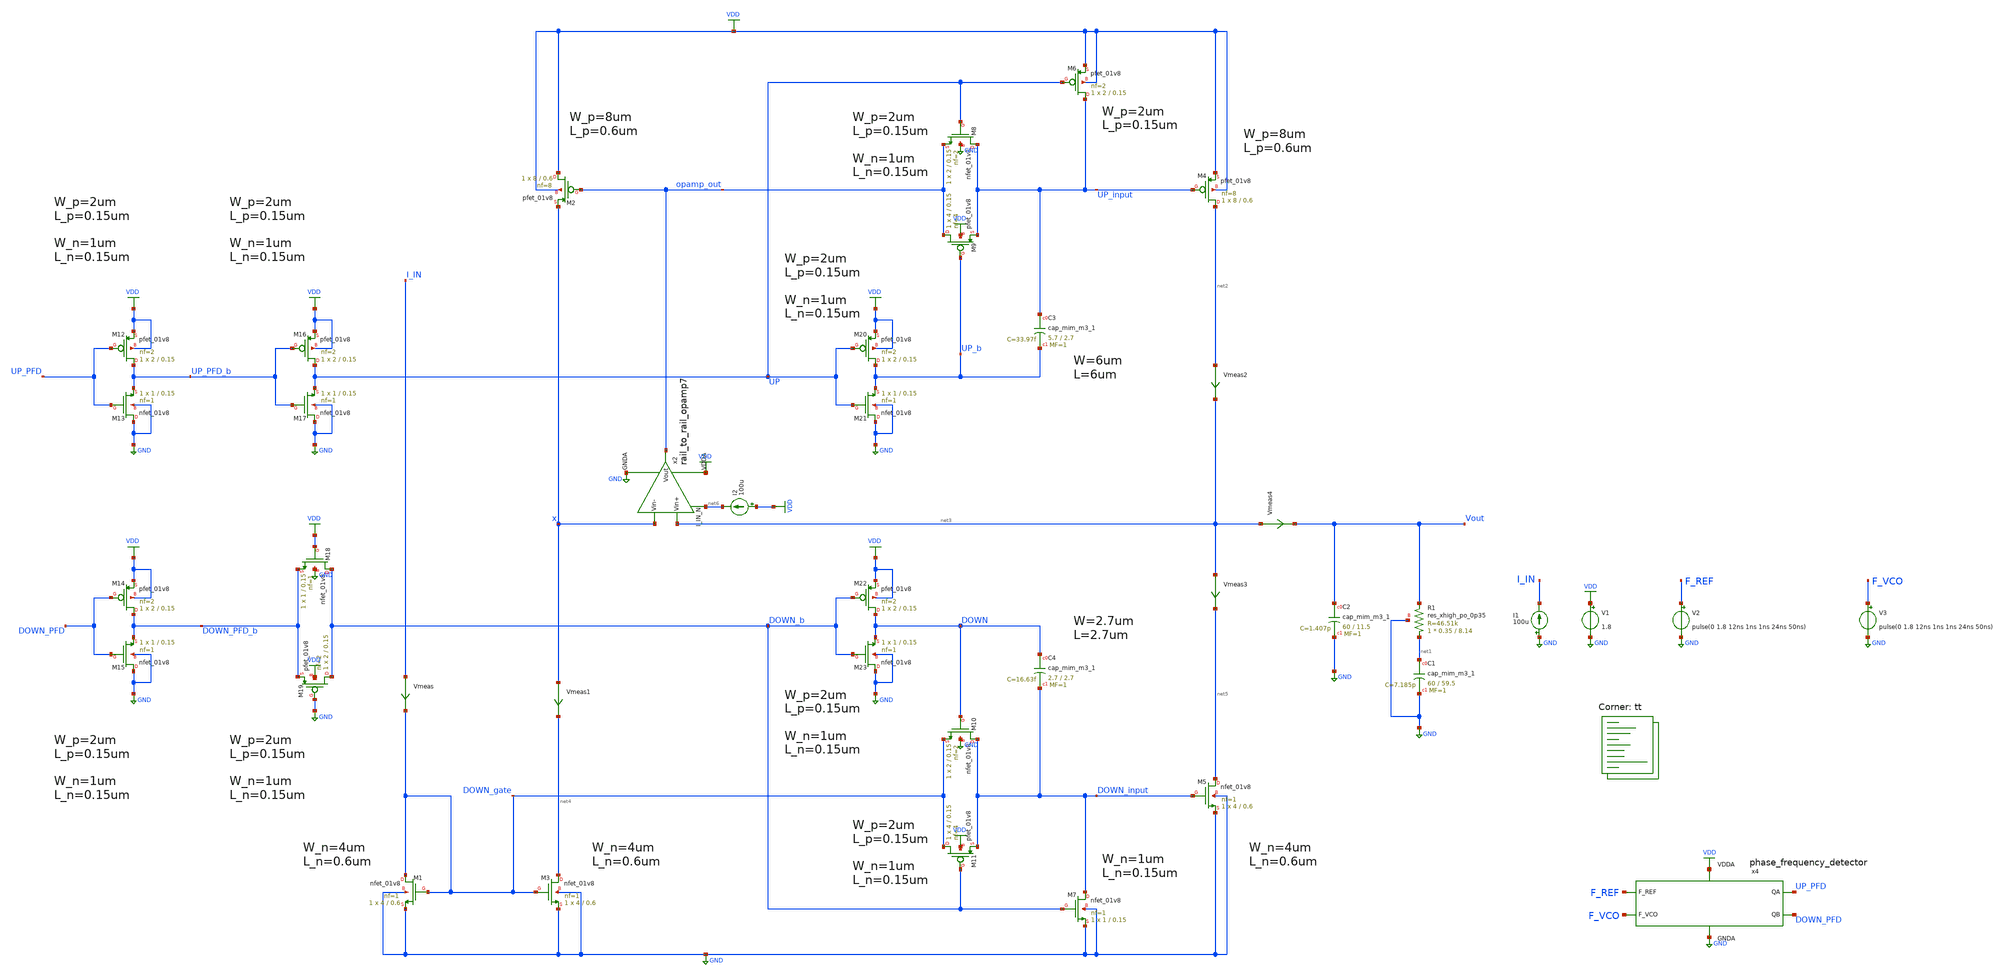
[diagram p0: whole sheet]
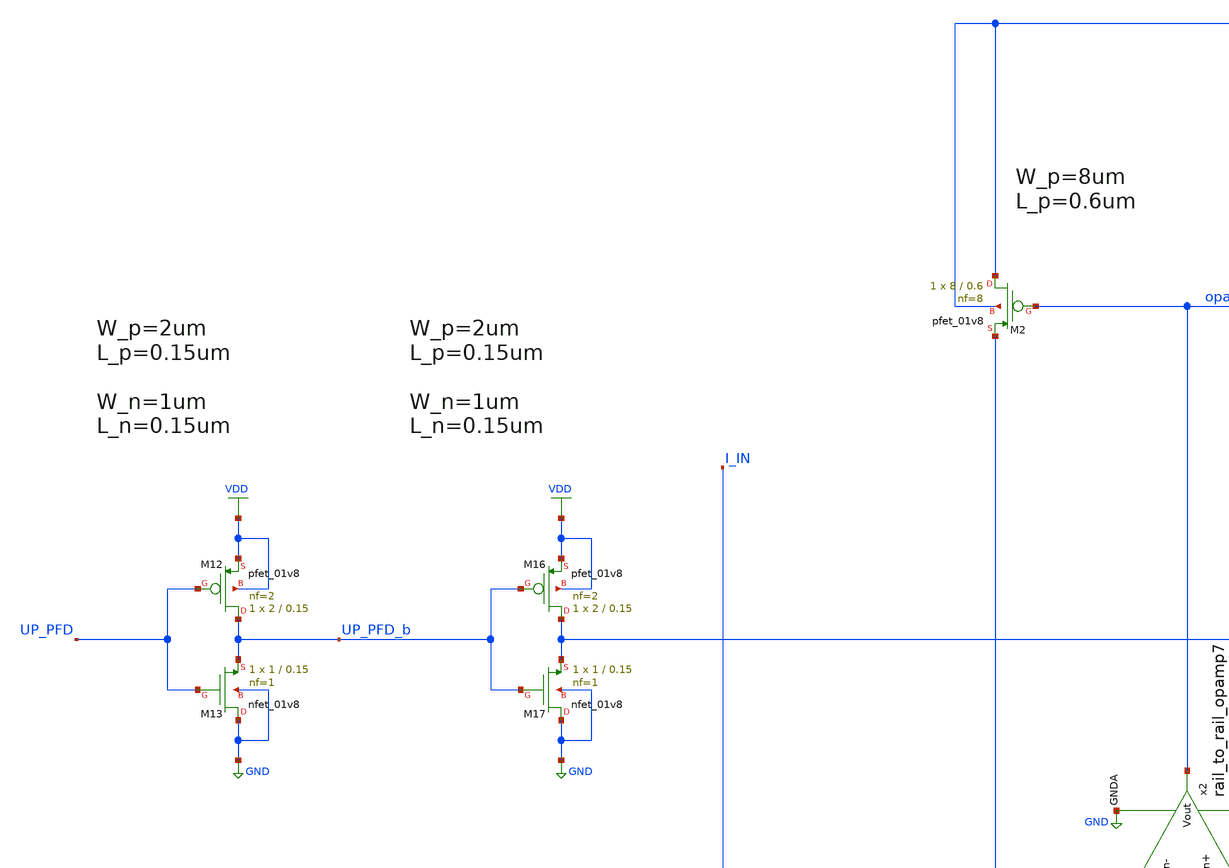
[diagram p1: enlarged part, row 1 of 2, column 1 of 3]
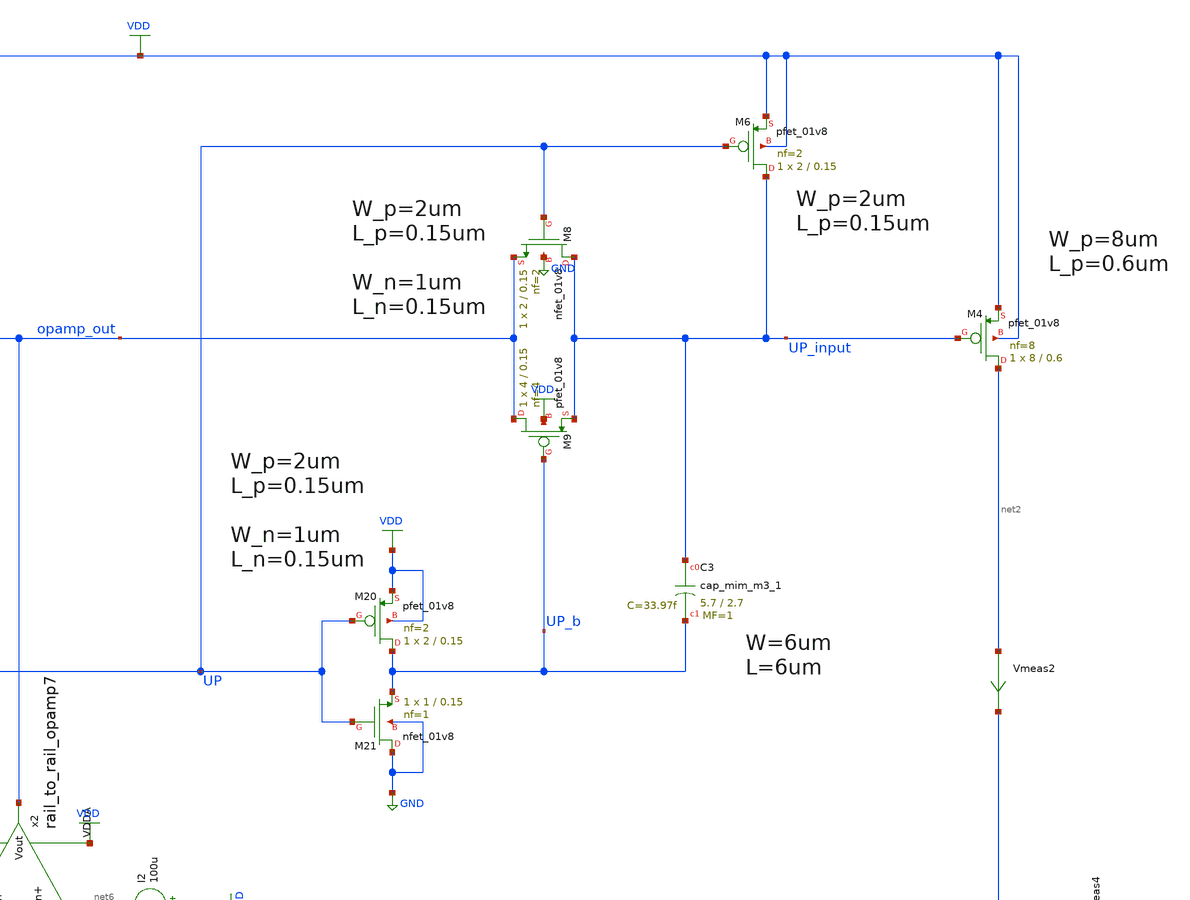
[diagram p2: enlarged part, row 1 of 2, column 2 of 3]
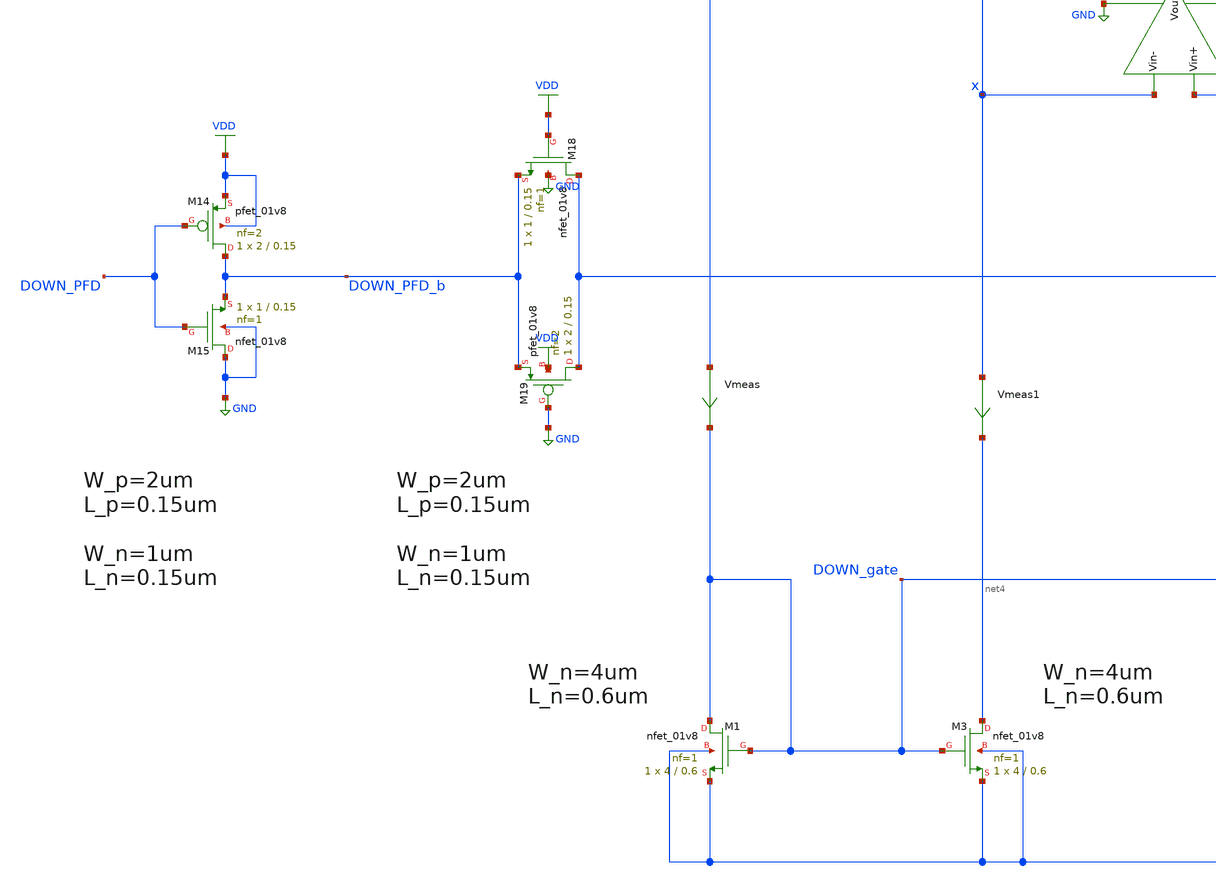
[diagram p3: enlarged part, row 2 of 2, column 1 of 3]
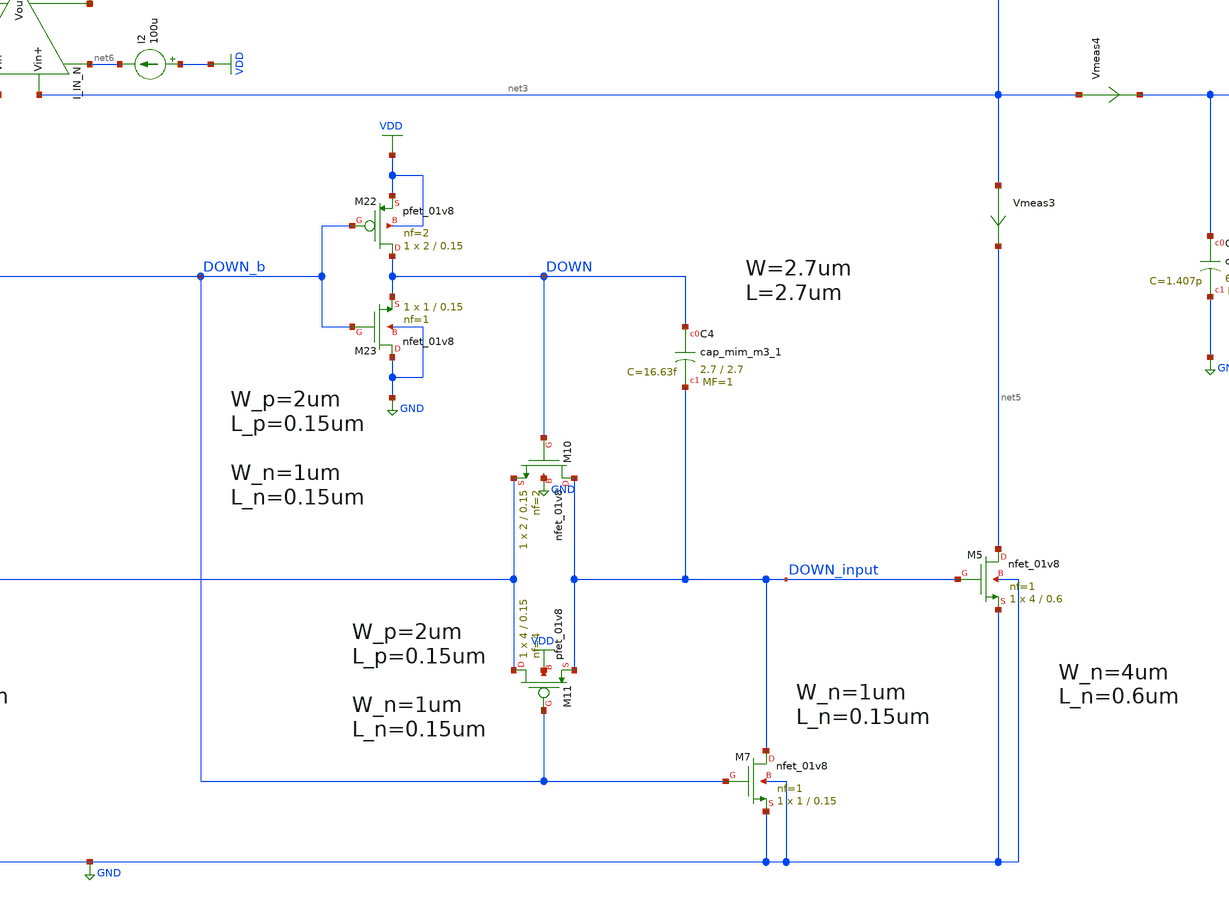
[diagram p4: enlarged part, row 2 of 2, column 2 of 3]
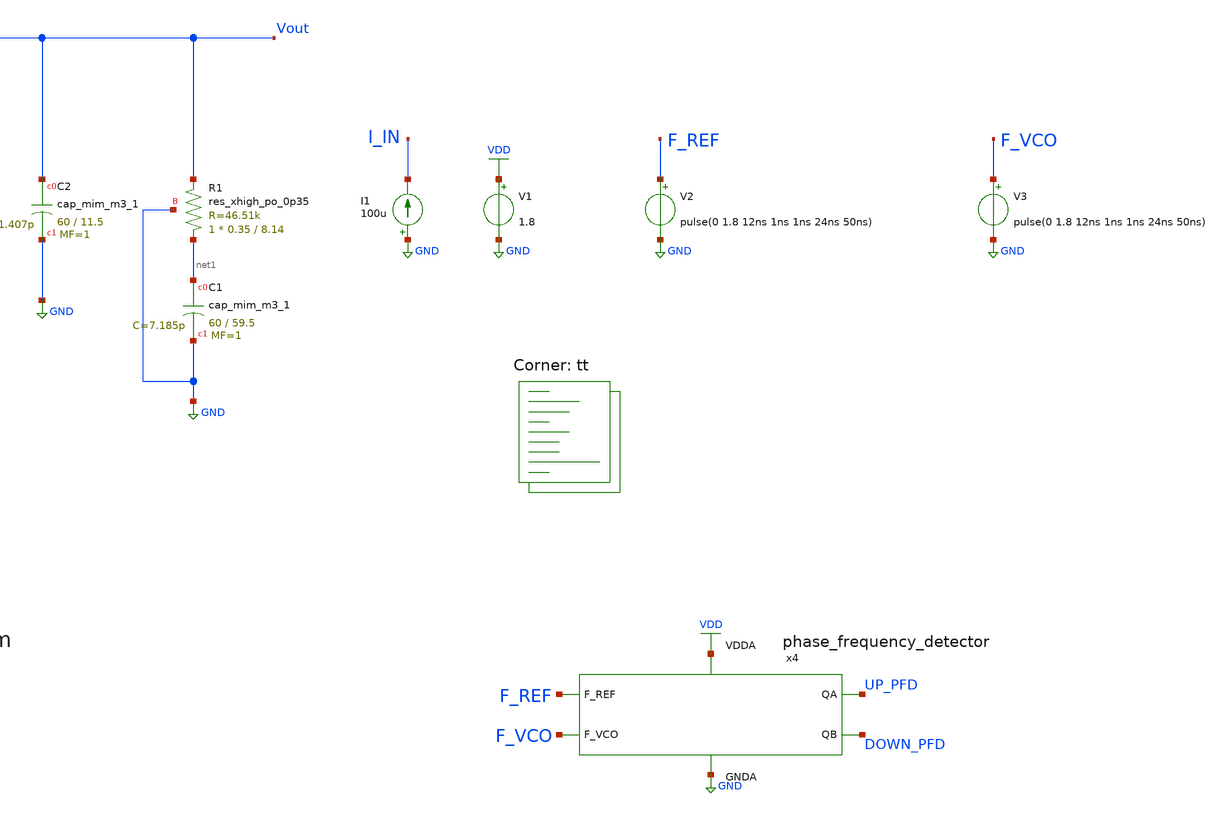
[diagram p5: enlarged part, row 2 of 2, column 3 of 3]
** sch_path: projects/pll/charge_pump/xschem_ngspice/pfd_charge_pump_13.sch
**.subckt pfd_charge_pump_13
V1 VDD GND 1.8
XC2 Vout GND sky130_fd_pr__cap_mim_m3_1 W=60 L=11.5 MF=1 m=1
XC1 net1 GND sky130_fd_pr__cap_mim_m3_1 W=60 L=59.5 MF=1 m=1
V2 F_REF GND pulse(0 1.8 12ns 1ns 1ns 24ns 50ns)
V3 F_VCO GND pulse(0 1.8 12ns 1ns 1ns 24ns 50ns)
x4 F_REF F_VCO VDD UP_PFD DOWN_PFD GND phase_frequency_detector
XR1 net1 Vout GND sky130_fd_pr__res_xhigh_po_0p35 L=8.14 mult=1 m=1
I1 GND I_IN 100u
Vmeas3 net3 net5 0
.save i(vmeas3)
XM1 DOWN_gate DOWN_gate GND GND sky130_fd_pr__nfet_01v8 L=0.6 W=4 nf=1 ad='int((nf+1)/2) * W/nf * 0.29'
+ as='int((nf+2)/2) * W/nf * 0.29' pd='2*int((nf+1)/2) * (W/nf + 0.29)' ps='2*int((nf+2)/2) * (W/nf + 0.29)'
+ nrd='0.29 / W' nrs='0.29 / W' sa=0 sb=0 sd=0 mult=1 m=1
XM3 net4 DOWN_gate GND GND sky130_fd_pr__nfet_01v8 L=0.6 W=4 nf=1 ad='int((nf+1)/2) * W/nf * 0.29' as='int((nf+2)/2) * W/nf * 0.29'
+ pd='2*int((nf+1)/2) * (W/nf + 0.29)' ps='2*int((nf+2)/2) * (W/nf + 0.29)' nrd='0.29 / W' nrs='0.29 / W'
+ sa=0 sb=0 sd=0 mult=1 m=1
XM2 VDD opamp_out x VDD sky130_fd_pr__pfet_01v8 L=0.6 W=8 nf=8 ad='int((nf+1)/2) * W/nf * 0.29' as='int((nf+2)/2) * W/nf * 0.29'
+ pd='2*int((nf+1)/2) * (W/nf + 0.29)' ps='2*int((nf+2)/2) * (W/nf + 0.29)' nrd='0.29 / W' nrs='0.29 / W'
+ sa=0 sb=0 sd=0 mult=1 m=1
XM9 opamp_out UP_b UP_input VDD sky130_fd_pr__pfet_01v8 L=0.15 W=4 nf=4 ad='int((nf+1)/2) * W/nf * 0.29'
+ as='int((nf+2)/2) * W/nf * 0.29' pd='2*int((nf+1)/2) * (W/nf + 0.29)' ps='2*int((nf+2)/2) * (W/nf + 0.29)'
+ nrd='0.29 / W' nrs='0.29 / W' sa=0 sb=0 sd=0 mult=1 m=1
XM6 UP_input UP VDD VDD sky130_fd_pr__pfet_01v8 L=0.15 W=2 nf=2 ad='int((nf+1)/2) * W/nf * 0.29' as='int((nf+2)/2) * W/nf * 0.29'
+ pd='2*int((nf+1)/2) * (W/nf + 0.29)' ps='2*int((nf+2)/2) * (W/nf + 0.29)' nrd='0.29 / W' nrs='0.29 / W'
+ sa=0 sb=0 sd=0 mult=1 m=1
XM4 net2 UP_input VDD VDD sky130_fd_pr__pfet_01v8 L=0.6 W=8 nf=8 ad='int((nf+1)/2) * W/nf * 0.29' as='int((nf+2)/2) * W/nf * 0.29'
+ pd='2*int((nf+1)/2) * (W/nf + 0.29)' ps='2*int((nf+2)/2) * (W/nf + 0.29)' nrd='0.29 / W' nrs='0.29 / W'
+ sa=0 sb=0 sd=0 mult=1 m=1
XM10 DOWN_input DOWN DOWN_gate GND sky130_fd_pr__nfet_01v8 L=0.15 W=2 nf=2 ad='int((nf+1)/2) * W/nf * 0.29'
+ as='int((nf+2)/2) * W/nf * 0.29' pd='2*int((nf+1)/2) * (W/nf + 0.29)' ps='2*int((nf+2)/2) * (W/nf + 0.29)'
+ nrd='0.29 / W' nrs='0.29 / W' sa=0 sb=0 sd=0 mult=1 m=1
XM7 DOWN_input DOWN_b GND GND sky130_fd_pr__nfet_01v8 L=0.15 W=1 nf=1 ad='int((nf+1)/2) * W/nf * 0.29'
+ as='int((nf+2)/2) * W/nf * 0.29' pd='2*int((nf+1)/2) * (W/nf + 0.29)' ps='2*int((nf+2)/2) * (W/nf + 0.29)'
+ nrd='0.29 / W' nrs='0.29 / W' sa=0 sb=0 sd=0 mult=1 m=1
XM5 net5 DOWN_input GND GND sky130_fd_pr__nfet_01v8 L=0.6 W=4 nf=1 ad='int((nf+1)/2) * W/nf * 0.29' as='int((nf+2)/2) * W/nf * 0.29'
+ pd='2*int((nf+1)/2) * (W/nf + 0.29)' ps='2*int((nf+2)/2) * (W/nf + 0.29)' nrd='0.29 / W' nrs='0.29 / W'
+ sa=0 sb=0 sd=0 mult=1 m=1
x2 net6 VDD net3 x opamp_out GND rail_to_rail_opamp7
XM19 DOWN_b GND DOWN_PFD_b VDD sky130_fd_pr__pfet_01v8 L=0.15 W=2 nf=2 ad='int((nf+1)/2) * W/nf * 0.29'
+ as='int((nf+2)/2) * W/nf * 0.29' pd='2*int((nf+1)/2) * (W/nf + 0.29)' ps='2*int((nf+2)/2) * (W/nf + 0.29)'
+ nrd='0.29 / W' nrs='0.29 / W' sa=0 sb=0 sd=0 mult=1 m=1
XM18 DOWN_b VDD DOWN_PFD_b GND sky130_fd_pr__nfet_01v8 L=0.15 W=1 nf=1 ad='int((nf+1)/2) * W/nf * 0.29'
+ as='int((nf+2)/2) * W/nf * 0.29' pd='2*int((nf+1)/2) * (W/nf + 0.29)' ps='2*int((nf+2)/2) * (W/nf + 0.29)'
+ nrd='0.29 / W' nrs='0.29 / W' sa=0 sb=0 sd=0 mult=1 m=1
XM14 DOWN_PFD_b DOWN_PFD VDD VDD sky130_fd_pr__pfet_01v8 L=0.15 W=2 nf=2 ad='int((nf+1)/2) * W/nf * 0.29'
+ as='int((nf+2)/2) * W/nf * 0.29' pd='2*int((nf+1)/2) * (W/nf + 0.29)' ps='2*int((nf+2)/2) * (W/nf + 0.29)'
+ nrd='0.29 / W' nrs='0.29 / W' sa=0 sb=0 sd=0 mult=1 m=1
XM15 GND DOWN_PFD DOWN_PFD_b GND sky130_fd_pr__nfet_01v8 L=0.15 W=1 nf=1 ad='int((nf+1)/2) * W/nf * 0.29'
+ as='int((nf+2)/2) * W/nf * 0.29' pd='2*int((nf+1)/2) * (W/nf + 0.29)' ps='2*int((nf+2)/2) * (W/nf + 0.29)'
+ nrd='0.29 / W' nrs='0.29 / W' sa=0 sb=0 sd=0 mult=1 m=1
XM12 UP_PFD_b UP_PFD VDD VDD sky130_fd_pr__pfet_01v8 L=0.15 W=2 nf=2 ad='int((nf+1)/2) * W/nf * 0.29'
+ as='int((nf+2)/2) * W/nf * 0.29' pd='2*int((nf+1)/2) * (W/nf + 0.29)' ps='2*int((nf+2)/2) * (W/nf + 0.29)'
+ nrd='0.29 / W' nrs='0.29 / W' sa=0 sb=0 sd=0 mult=1 m=1
XM13 GND UP_PFD UP_PFD_b GND sky130_fd_pr__nfet_01v8 L=0.15 W=1 nf=1 ad='int((nf+1)/2) * W/nf * 0.29'
+ as='int((nf+2)/2) * W/nf * 0.29' pd='2*int((nf+1)/2) * (W/nf + 0.29)' ps='2*int((nf+2)/2) * (W/nf + 0.29)'
+ nrd='0.29 / W' nrs='0.29 / W' sa=0 sb=0 sd=0 mult=1 m=1
XM16 UP UP_PFD_b VDD VDD sky130_fd_pr__pfet_01v8 L=0.15 W=2 nf=2 ad='int((nf+1)/2) * W/nf * 0.29' as='int((nf+2)/2) * W/nf * 0.29'
+ pd='2*int((nf+1)/2) * (W/nf + 0.29)' ps='2*int((nf+2)/2) * (W/nf + 0.29)' nrd='0.29 / W' nrs='0.29 / W'
+ sa=0 sb=0 sd=0 mult=1 m=1
XM17 GND UP_PFD_b UP GND sky130_fd_pr__nfet_01v8 L=0.15 W=1 nf=1 ad='int((nf+1)/2) * W/nf * 0.29' as='int((nf+2)/2) * W/nf * 0.29'
+ pd='2*int((nf+1)/2) * (W/nf + 0.29)' ps='2*int((nf+2)/2) * (W/nf + 0.29)' nrd='0.29 / W' nrs='0.29 / W'
+ sa=0 sb=0 sd=0 mult=1 m=1
XM22 DOWN DOWN_b VDD VDD sky130_fd_pr__pfet_01v8 L=0.15 W=2 nf=2 ad='int((nf+1)/2) * W/nf * 0.29' as='int((nf+2)/2) * W/nf * 0.29'
+ pd='2*int((nf+1)/2) * (W/nf + 0.29)' ps='2*int((nf+2)/2) * (W/nf + 0.29)' nrd='0.29 / W' nrs='0.29 / W'
+ sa=0 sb=0 sd=0 mult=1 m=1
XM23 GND DOWN_b DOWN GND sky130_fd_pr__nfet_01v8 L=0.15 W=1 nf=1 ad='int((nf+1)/2) * W/nf * 0.29' as='int((nf+2)/2) * W/nf * 0.29'
+ pd='2*int((nf+1)/2) * (W/nf + 0.29)' ps='2*int((nf+2)/2) * (W/nf + 0.29)' nrd='0.29 / W' nrs='0.29 / W'
+ sa=0 sb=0 sd=0 mult=1 m=1
XM20 UP_b UP VDD VDD sky130_fd_pr__pfet_01v8 L=0.15 W=2 nf=2 ad='int((nf+1)/2) * W/nf * 0.29' as='int((nf+2)/2) * W/nf * 0.29'
+ pd='2*int((nf+1)/2) * (W/nf + 0.29)' ps='2*int((nf+2)/2) * (W/nf + 0.29)' nrd='0.29 / W' nrs='0.29 / W'
+ sa=0 sb=0 sd=0 mult=1 m=1
XM21 GND UP UP_b GND sky130_fd_pr__nfet_01v8 L=0.15 W=1 nf=1 ad='int((nf+1)/2) * W/nf * 0.29' as='int((nf+2)/2) * W/nf * 0.29'
+ pd='2*int((nf+1)/2) * (W/nf + 0.29)' ps='2*int((nf+2)/2) * (W/nf + 0.29)' nrd='0.29 / W' nrs='0.29 / W'
+ sa=0 sb=0 sd=0 mult=1 m=1
Vmeas I_IN DOWN_gate 0
.save i(vmeas)
Vmeas1 x net4 0
.save i(vmeas1)
Vmeas2 net2 net3 0
.save i(vmeas2)
Vmeas4 net3 Vout 0
.save i(vmeas4)
XM8 UP_input UP opamp_out GND sky130_fd_pr__nfet_01v8 L=0.15 W=2 nf=2 ad='int((nf+1)/2) * W/nf * 0.29'
+ as='int((nf+2)/2) * W/nf * 0.29' pd='2*int((nf+1)/2) * (W/nf + 0.29)' ps='2*int((nf+2)/2) * (W/nf + 0.29)'
+ nrd='0.29 / W' nrs='0.29 / W' sa=0 sb=0 sd=0 mult=1 m=1
XM11 DOWN_gate DOWN_b DOWN_input VDD sky130_fd_pr__pfet_01v8 L=0.15 W=4 nf=4 ad='int((nf+1)/2) * W/nf * 0.29'
+ as='int((nf+2)/2) * W/nf * 0.29' pd='2*int((nf+1)/2) * (W/nf + 0.29)' ps='2*int((nf+2)/2) * (W/nf + 0.29)'
+ nrd='0.29 / W' nrs='0.29 / W' sa=0 sb=0 sd=0 mult=1 m=1
XC3 UP_input UP_b sky130_fd_pr__cap_mim_m3_1 W=5.7 L=2.7 MF=1 m=1
XC4 DOWN DOWN_input sky130_fd_pr__cap_mim_m3_1 W=2.7 L=2.7 MF=1 m=1
I2 VDD net6 100u
**** begin user architecture code
.lib $::SKYWATER_MODELS/sky130.lib.spice tt



.include /foss/pdks/sky130A/libs.ref/sky130_fd_sc_hd/spice/sky130_fd_sc_hd.spice

.option method=gear
.option wnflag=1
.option savecurrents

.save @m.x2.xm11.msky130_fd_pr__pfet_01v8[gm] @m.x2.xm12.msky130_fd_pr__nfet_01v8[gm]

* V_out initial voltage value for the F_VCO delay of 2ns  (leading)
* .ic v(vout) = 1.8

* V_out initial voltage value for the F_VCO delay of 12ns (lock condition)
.ic v(vout) = 0.83

* V_out initial voltage value for the F_VCO delay of 22ns (lagging)
* .ic v(vout) = 0

.control
  * save v(f_ref) save v(f_vco) save v(i_in) save v(up_pfd) v(down_pfd) v(up_pfd_b) v(down_pfd_b)
+ v(up) v(up_b) v(down) v(down_b) v(x) v(opamp_out) v(up_input) v(down_input) v(down_gate) v(vout)
  save all

  * timestep for exact simulation results
  * tran 5ps 0.5us

  * timestep for faster simulation results
  tran 50ps 0.5us

  remzerovec
  * write pfd_charge_pump_13.raw
  write pfd_charge_pump_13_2.raw
  set appendwrite

.endc



**** end user architecture code
**.ends

* expanding   symbol:
*+  /foss/designs/my_design/projects/pll/pfd/xschem_ngspice/phase_frequency_detector.sym # of pins=6
** sym_path: projects/pll/pfd/xschem_ngspice/phase_frequency_detector.sym
** sch_path: projects/pll/pfd/xschem_ngspice/phase_frequency_detector.sch
.subckt phase_frequency_detector F_REF F_VCO VDDA QA QB GNDA
*.ipin F_REF
*.opin QA
*.ipin F_VCO
*.opin QB
*.ipin VDDA
*.ipin GNDA
x1 F_REF QA GNDA GNDA VDDA VDDA QA_b sky130_fd_sc_hd__nor2_1
x2 QA_b E GNDA GNDA VDDA VDDA QA sky130_fd_sc_hd__nor2_1
x3 QA_b E_b GNDA GNDA VDDA VDDA E sky130_fd_sc_hd__nor2_1
x4 E Reset GNDA GNDA VDDA VDDA E_b sky130_fd_sc_hd__nor2_1
x5 F_VCO QB GNDA GNDA VDDA VDDA QB_b sky130_fd_sc_hd__nor2_1
x6 QB_b F GNDA GNDA VDDA VDDA QB sky130_fd_sc_hd__nor2_1
x7 QB_b F_b GNDA GNDA VDDA VDDA F sky130_fd_sc_hd__nor2_1
x8 F Reset GNDA GNDA VDDA VDDA F_b sky130_fd_sc_hd__nor2_1
x9 QA QB GNDA GNDA VDDA VDDA before_Reset sky130_fd_sc_hd__nand2_1
x10 before_Reset GNDA GNDA VDDA VDDA net1 sky130_fd_sc_hd__inv_1
x11 net1 GNDA GNDA VDDA VDDA net2 sky130_fd_sc_hd__inv_1
x12 net2 GNDA GNDA VDDA VDDA net3 sky130_fd_sc_hd__inv_1
x13 net3 GNDA GNDA VDDA VDDA net4 sky130_fd_sc_hd__inv_1
x14 net4 GNDA GNDA VDDA VDDA Reset sky130_fd_sc_hd__inv_1
.ends


* expanding   symbol:
*+  /foss/designs/my_design/projects/pll/charge_pump/xschem_ngspice/rail_to_rail_opamp7.sym # of pins=6
** sym_path: projects/pll/charge_pump/xschem_ngspice/rail_to_rail_opamp7.sym
** sch_path: projects/pll/charge_pump/xschem_ngspice/rail_to_rail_opamp7.sch
.subckt rail_to_rail_opamp7 I_IN_N VDDA Vin+ Vin- Vout GNDA
*.opin Vout
*.ipin Vin+
*.ipin Vin-
*.ipin VDDA
*.ipin GNDA
*.ipin I_IN_N
XM2 n_left Vin+ v_common_n GNDA sky130_fd_pr__nfet_01v8 L=0.15 W=1 nf=1 ad='int((nf+1)/2) * W/nf * 0.29'
+ as='int((nf+2)/2) * W/nf * 0.29' pd='2*int((nf+1)/2) * (W/nf + 0.29)' ps='2*int((nf+2)/2) * (W/nf + 0.29)'
+ nrd='0.29 / W' nrs='0.29 / W' sa=0 sb=0 sd=0 mult=1 m=1
XM3 n_right Vin- v_common_n GNDA sky130_fd_pr__nfet_01v8 L=0.15 W=1 nf=1 ad='int((nf+1)/2) * W/nf * 0.29'
+ as='int((nf+2)/2) * W/nf * 0.29' pd='2*int((nf+1)/2) * (W/nf + 0.29)' ps='2*int((nf+2)/2) * (W/nf + 0.29)'
+ nrd='0.29 / W' nrs='0.29 / W' sa=0 sb=0 sd=0 mult=1 m=1
XM5 n_left n_left VDDA VDDA sky130_fd_pr__pfet_01v8 L=0.15 W=2 nf=2 ad='int((nf+1)/2) * W/nf * 0.29'
+ as='int((nf+2)/2) * W/nf * 0.29' pd='2*int((nf+1)/2) * (W/nf + 0.29)' ps='2*int((nf+2)/2) * (W/nf + 0.29)'
+ nrd='0.29 / W' nrs='0.29 / W' sa=0 sb=0 sd=0 mult=1 m=1
XM4 n_right n_left VDDA VDDA sky130_fd_pr__pfet_01v8 L=0.15 W=2 nf=2 ad='int((nf+1)/2) * W/nf * 0.29'
+ as='int((nf+2)/2) * W/nf * 0.29' pd='2*int((nf+1)/2) * (W/nf + 0.29)' ps='2*int((nf+2)/2) * (W/nf + 0.29)'
+ nrd='0.29 / W' nrs='0.29 / W' sa=0 sb=0 sd=0 mult=1 m=1
XM6 v_common_p top_gate VDDA VDDA sky130_fd_pr__pfet_01v8 L=0.15 W=2 nf=2 ad='int((nf+1)/2) * W/nf * 0.29'
+ as='int((nf+2)/2) * W/nf * 0.29' pd='2*int((nf+1)/2) * (W/nf + 0.29)' ps='2*int((nf+2)/2) * (W/nf + 0.29)'
+ nrd='0.29 / W' nrs='0.29 / W' sa=0 sb=0 sd=0 mult=1 m=1
XM7 p_left Vin+ v_common_p VDDA sky130_fd_pr__pfet_01v8 L=0.15 W=2 nf=2 ad='int((nf+1)/2) * W/nf * 0.29'
+ as='int((nf+2)/2) * W/nf * 0.29' pd='2*int((nf+1)/2) * (W/nf + 0.29)' ps='2*int((nf+2)/2) * (W/nf + 0.29)'
+ nrd='0.29 / W' nrs='0.29 / W' sa=0 sb=0 sd=0 mult=1 m=1
XM8 p_right Vin- v_common_p VDDA sky130_fd_pr__pfet_01v8 L=0.15 W=2 nf=2 ad='int((nf+1)/2) * W/nf * 0.29'
+ as='int((nf+2)/2) * W/nf * 0.29' pd='2*int((nf+1)/2) * (W/nf + 0.29)' ps='2*int((nf+2)/2) * (W/nf + 0.29)'
+ nrd='0.29 / W' nrs='0.29 / W' sa=0 sb=0 sd=0 mult=1 m=1
XM9 p_left p_left GNDA GNDA sky130_fd_pr__nfet_01v8 L=0.15 W=1 nf=1 ad='int((nf+1)/2) * W/nf * 0.29'
+ as='int((nf+2)/2) * W/nf * 0.29' pd='2*int((nf+1)/2) * (W/nf + 0.29)' ps='2*int((nf+2)/2) * (W/nf + 0.29)'
+ nrd='0.29 / W' nrs='0.29 / W' sa=0 sb=0 sd=0 mult=1 m=1
XM10 p_right p_left GNDA GNDA sky130_fd_pr__nfet_01v8 L=0.15 W=1 nf=1 ad='int((nf+1)/2) * W/nf * 0.29'
+ as='int((nf+2)/2) * W/nf * 0.29' pd='2*int((nf+1)/2) * (W/nf + 0.29)' ps='2*int((nf+2)/2) * (W/nf + 0.29)'
+ nrd='0.29 / W' nrs='0.29 / W' sa=0 sb=0 sd=0 mult=1 m=1
XM1 v_common_n I_IN_N GNDA GNDA sky130_fd_pr__nfet_01v8 L=0.15 W=1 nf=1 ad='int((nf+1)/2) * W/nf * 0.29'
+ as='int((nf+2)/2) * W/nf * 0.29' pd='2*int((nf+1)/2) * (W/nf + 0.29)' ps='2*int((nf+2)/2) * (W/nf + 0.29)'
+ nrd='0.29 / W' nrs='0.29 / W' sa=0 sb=0 sd=0 mult=1 m=1
XM11 Vout n_right VDDA VDDA sky130_fd_pr__pfet_01v8 L=0.15 W=2 nf=2 ad='int((nf+1)/2) * W/nf * 0.29'
+ as='int((nf+2)/2) * W/nf * 0.29' pd='2*int((nf+1)/2) * (W/nf + 0.29)' ps='2*int((nf+2)/2) * (W/nf + 0.29)'
+ nrd='0.29 / W' nrs='0.29 / W' sa=0 sb=0 sd=0 mult=1 m=1
XM12 Vout p_right GNDA GNDA sky130_fd_pr__nfet_01v8 L=0.15 W=1 nf=1 ad='int((nf+1)/2) * W/nf * 0.29'
+ as='int((nf+2)/2) * W/nf * 0.29' pd='2*int((nf+1)/2) * (W/nf + 0.29)' ps='2*int((nf+2)/2) * (W/nf + 0.29)'
+ nrd='0.29 / W' nrs='0.29 / W' sa=0 sb=0 sd=0 mult=1 m=1
XM13 I_IN_N I_IN_N GNDA GNDA sky130_fd_pr__nfet_01v8 L=0.15 W=1 nf=1 ad='int((nf+1)/2) * W/nf * 0.29'
+ as='int((nf+2)/2) * W/nf * 0.29' pd='2*int((nf+1)/2) * (W/nf + 0.29)' ps='2*int((nf+2)/2) * (W/nf + 0.29)'
+ nrd='0.29 / W' nrs='0.29 / W' sa=0 sb=0 sd=0 mult=1 m=1
XM15 top_gate top_gate VDDA VDDA sky130_fd_pr__pfet_01v8 L=0.15 W=2 nf=2 ad='int((nf+1)/2) * W/nf * 0.29'
+ as='int((nf+2)/2) * W/nf * 0.29' pd='2*int((nf+1)/2) * (W/nf + 0.29)' ps='2*int((nf+2)/2) * (W/nf + 0.29)'
+ nrd='0.29 / W' nrs='0.29 / W' sa=0 sb=0 sd=0 mult=1 m=1
XM14 top_gate I_IN_N GNDA GNDA sky130_fd_pr__nfet_01v8 L=0.15 W=1 nf=1 ad='int((nf+1)/2) * W/nf * 0.29'
+ as='int((nf+2)/2) * W/nf * 0.29' pd='2*int((nf+1)/2) * (W/nf + 0.29)' ps='2*int((nf+2)/2) * (W/nf + 0.29)'
+ nrd='0.29 / W' nrs='0.29 / W' sa=0 sb=0 sd=0 mult=1 m=1
XC1 n_right net1 sky130_fd_pr__cap_mim_m3_1 W=10 L=10 MF=1 m=1
XC2 p_right net2 sky130_fd_pr__cap_mim_m3_1 W=10 L=10 MF=1 m=1
XR1 Vout net1 GNDA sky130_fd_pr__res_xhigh_po_0p35 L=1.6 mult=1 m=1
XR2 net2 Vout GNDA sky130_fd_pr__res_xhigh_po_0p35 L=1.1 mult=1 m=1
.ends

.GLOBAL GND
.GLOBAL VDD
.end
